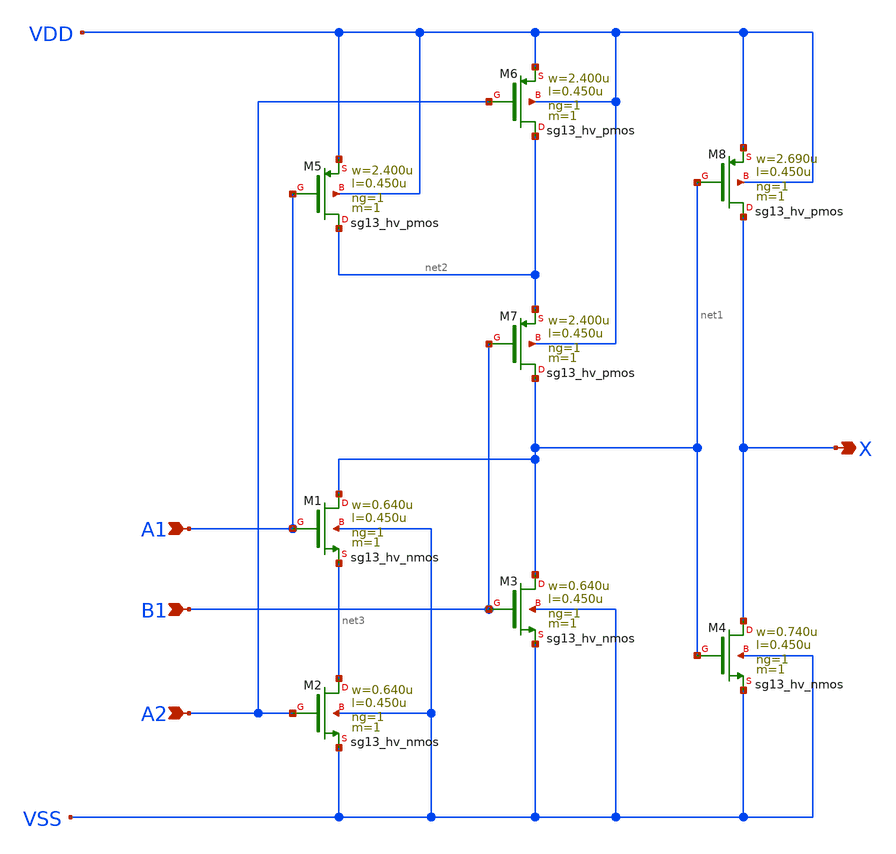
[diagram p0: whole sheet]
** sch_path: ihp-sg13g2/libs.ref/sg13g2_stdcell_hv/sch/xschem/sg13g2_hv_a21o_1.sch
**.subckt sg13g2_hv_a21o_1 X A1 A2 B1
*.opin X
*.ipin A1
*.ipin A2
*.ipin B1
XM1 net1 A1 net3 VSS sg13_hv_nmos w=0.640u l=0.450u ng=1 m=1 mm_ok=1
XM2 net3 A2 VSS VSS sg13_hv_nmos w=0.640u l=0.450u ng=1 m=1 mm_ok=1
XM3 net1 B1 VSS VSS sg13_hv_nmos w=0.640u l=0.450u ng=1 m=1 mm_ok=1
XM4 X net1 VSS VSS sg13_hv_nmos w=0.740u l=0.450u ng=1 m=1 mm_ok=1
XM5 net2 A1 VDD VDD sg13_hv_pmos w=2.400u l=0.450u ng=1 m=1 mm_ok=1
XM6 net2 A2 VDD VDD sg13_hv_pmos w=2.400u l=0.450u ng=1 m=1 mm_ok=1
XM7 net1 B1 net2 VDD sg13_hv_pmos w=2.400u l=0.450u ng=1 m=1 mm_ok=1
XM8 X net1 VDD VDD sg13_hv_pmos w=2.690u l=0.450u ng=1 m=1 mm_ok=1
**.ends
.end
